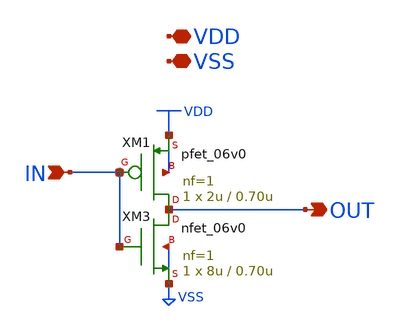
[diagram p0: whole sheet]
** sch_path: xschem/io_inv_1i.sch
* Copyright 2023 David Mitchell Bailey
* Licensed under the Apache License, Version 2.0 (the "License");
* you may not use this file except in compliance with the License.
* You may obtain a copy of the License at
* https://www.apache.org/licenses/LICENSE-2.0
* Unless required by applicable law or agreed to in writing, software
* distributed under the License is distributed on an "AS IS" BASIS,
* WITHOUT WARRANTIES OR CONDITIONS OF ANY KIND, either express or implied.
* See the License for the specific language governing permissions and
* limitations under the License.
**.subckt io_inv_1i OUT IN VDD VSS
*.opin OUT
*.ipin IN
*.iopin VDD
*.iopin VSS
XM1 OUT IN VDD VDD pfet_06v0 L=0.70u W=2u nf=1 ad='int((nf+1)/2) * W/nf * 0.18u' as='int((nf+2)/2) * W/nf * 0.18u'
+ pd='2*int((nf+1)/2) * (W/nf + 0.18u)' ps='2*int((nf+2)/2) * (W/nf + 0.18u)' nrd='0.18u / W' nrs='0.18u / W'
+ sa=0 sb=0 sd=0 m=1
XM3 OUT IN VSS VSS nfet_06v0 L=0.70u W=8u nf=1 ad='int((nf+1)/2) * W/nf * 0.18u' as='int((nf+2)/2) * W/nf * 0.18u'
+ pd='2*int((nf+1)/2) * (W/nf + 0.18u)' ps='2*int((nf+2)/2) * (W/nf + 0.18u)' nrd='0.18u / W' nrs='0.18u / W'
+ sa=0 sb=0 sd=0 m=1 par=1
**.ends
.GLOBAL VDD
.end
